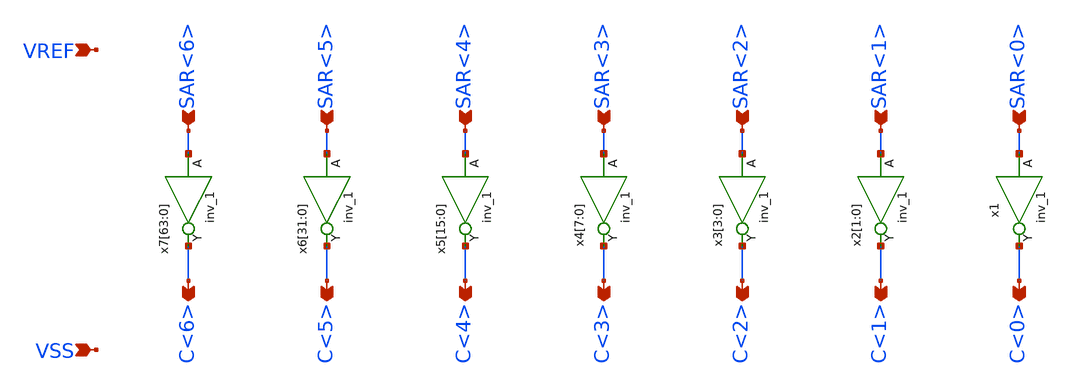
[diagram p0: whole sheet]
** sch_path: module/cdac2/cdac_drv.sch
**.subckt cdac_drv VREF VSS SAR<6> SAR<5> SAR<4> SAR<3> SAR<2> SAR<1> SAR<0> C<6> C<5> C<4> C<3>
*+ C<2> C<1> C<0>
*.ipin VREF
*.ipin VSS
*.ipin SAR<6>
*.ipin SAR<5>
*.ipin SAR<4>
*.ipin SAR<3>
*.ipin SAR<2>
*.ipin SAR<1>
*.ipin SAR<0>
*.opin C<6>
*.opin C<5>
*.opin C<4>
*.opin C<3>
*.opin C<2>
*.opin C<1>
*.opin C<0>
x2[1] SAR<1> VSS VSS VDD VREF C<1> sky130_fd_sc_hd__inv_1
x2[0] SAR<1> VSS VSS VDD VREF C<1> sky130_fd_sc_hd__inv_1
x1 SAR<0> VSS VSS VDD VPWR C<0> sky130_fd_sc_hd__inv_1
x3[3] SAR<2> VSS VSS VDD VREF C<2> sky130_fd_sc_hd__inv_1
x3[2] SAR<2> VSS VSS VDD VREF C<2> sky130_fd_sc_hd__inv_1
x3[1] SAR<2> VSS VSS VDD VREF C<2> sky130_fd_sc_hd__inv_1
x3[0] SAR<2> VSS VSS VDD VREF C<2> sky130_fd_sc_hd__inv_1
x4[7] SAR<3> VSS VSS VDD VREF C<3> sky130_fd_sc_hd__inv_1
x4[6] SAR<3> VSS VSS VDD VREF C<3> sky130_fd_sc_hd__inv_1
x4[5] SAR<3> VSS VSS VDD VREF C<3> sky130_fd_sc_hd__inv_1
x4[4] SAR<3> VSS VSS VDD VREF C<3> sky130_fd_sc_hd__inv_1
x4[3] SAR<3> VSS VSS VDD VREF C<3> sky130_fd_sc_hd__inv_1
x4[2] SAR<3> VSS VSS VDD VREF C<3> sky130_fd_sc_hd__inv_1
x4[1] SAR<3> VSS VSS VDD VREF C<3> sky130_fd_sc_hd__inv_1
x4[0] SAR<3> VSS VSS VDD VREF C<3> sky130_fd_sc_hd__inv_1
x5[15] SAR<4> VSS VSS VDD VREF C<4> sky130_fd_sc_hd__inv_1
x5[14] SAR<4> VSS VSS VDD VREF C<4> sky130_fd_sc_hd__inv_1
x5[13] SAR<4> VSS VSS VDD VREF C<4> sky130_fd_sc_hd__inv_1
x5[12] SAR<4> VSS VSS VDD VREF C<4> sky130_fd_sc_hd__inv_1
x5[11] SAR<4> VSS VSS VDD VREF C<4> sky130_fd_sc_hd__inv_1
x5[10] SAR<4> VSS VSS VDD VREF C<4> sky130_fd_sc_hd__inv_1
x5[9] SAR<4> VSS VSS VDD VREF C<4> sky130_fd_sc_hd__inv_1
x5[8] SAR<4> VSS VSS VDD VREF C<4> sky130_fd_sc_hd__inv_1
x5[7] SAR<4> VSS VSS VDD VREF C<4> sky130_fd_sc_hd__inv_1
x5[6] SAR<4> VSS VSS VDD VREF C<4> sky130_fd_sc_hd__inv_1
x5[5] SAR<4> VSS VSS VDD VREF C<4> sky130_fd_sc_hd__inv_1
x5[4] SAR<4> VSS VSS VDD VREF C<4> sky130_fd_sc_hd__inv_1
x5[3] SAR<4> VSS VSS VDD VREF C<4> sky130_fd_sc_hd__inv_1
x5[2] SAR<4> VSS VSS VDD VREF C<4> sky130_fd_sc_hd__inv_1
x5[1] SAR<4> VSS VSS VDD VREF C<4> sky130_fd_sc_hd__inv_1
x5[0] SAR<4> VSS VSS VDD VREF C<4> sky130_fd_sc_hd__inv_1
x6[31] SAR<5> VSS VSS VDD VREF C<5> sky130_fd_sc_hd__inv_1
x6[30] SAR<5> VSS VSS VDD VREF C<5> sky130_fd_sc_hd__inv_1
x6[29] SAR<5> VSS VSS VDD VREF C<5> sky130_fd_sc_hd__inv_1
x6[28] SAR<5> VSS VSS VDD VREF C<5> sky130_fd_sc_hd__inv_1
x6[27] SAR<5> VSS VSS VDD VREF C<5> sky130_fd_sc_hd__inv_1
x6[26] SAR<5> VSS VSS VDD VREF C<5> sky130_fd_sc_hd__inv_1
x6[25] SAR<5> VSS VSS VDD VREF C<5> sky130_fd_sc_hd__inv_1
x6[24] SAR<5> VSS VSS VDD VREF C<5> sky130_fd_sc_hd__inv_1
x6[23] SAR<5> VSS VSS VDD VREF C<5> sky130_fd_sc_hd__inv_1
x6[22] SAR<5> VSS VSS VDD VREF C<5> sky130_fd_sc_hd__inv_1
x6[21] SAR<5> VSS VSS VDD VREF C<5> sky130_fd_sc_hd__inv_1
x6[20] SAR<5> VSS VSS VDD VREF C<5> sky130_fd_sc_hd__inv_1
x6[19] SAR<5> VSS VSS VDD VREF C<5> sky130_fd_sc_hd__inv_1
x6[18] SAR<5> VSS VSS VDD VREF C<5> sky130_fd_sc_hd__inv_1
x6[17] SAR<5> VSS VSS VDD VREF C<5> sky130_fd_sc_hd__inv_1
x6[16] SAR<5> VSS VSS VDD VREF C<5> sky130_fd_sc_hd__inv_1
x6[15] SAR<5> VSS VSS VDD VREF C<5> sky130_fd_sc_hd__inv_1
x6[14] SAR<5> VSS VSS VDD VREF C<5> sky130_fd_sc_hd__inv_1
x6[13] SAR<5> VSS VSS VDD VREF C<5> sky130_fd_sc_hd__inv_1
x6[12] SAR<5> VSS VSS VDD VREF C<5> sky130_fd_sc_hd__inv_1
x6[11] SAR<5> VSS VSS VDD VREF C<5> sky130_fd_sc_hd__inv_1
x6[10] SAR<5> VSS VSS VDD VREF C<5> sky130_fd_sc_hd__inv_1
x6[9] SAR<5> VSS VSS VDD VREF C<5> sky130_fd_sc_hd__inv_1
x6[8] SAR<5> VSS VSS VDD VREF C<5> sky130_fd_sc_hd__inv_1
x6[7] SAR<5> VSS VSS VDD VREF C<5> sky130_fd_sc_hd__inv_1
x6[6] SAR<5> VSS VSS VDD VREF C<5> sky130_fd_sc_hd__inv_1
x6[5] SAR<5> VSS VSS VDD VREF C<5> sky130_fd_sc_hd__inv_1
x6[4] SAR<5> VSS VSS VDD VREF C<5> sky130_fd_sc_hd__inv_1
x6[3] SAR<5> VSS VSS VDD VREF C<5> sky130_fd_sc_hd__inv_1
x6[2] SAR<5> VSS VSS VDD VREF C<5> sky130_fd_sc_hd__inv_1
x6[1] SAR<5> VSS VSS VDD VREF C<5> sky130_fd_sc_hd__inv_1
x6[0] SAR<5> VSS VSS VDD VREF C<5> sky130_fd_sc_hd__inv_1
x7[63] SAR<6> VSS VSS VDD VREF C<6> sky130_fd_sc_hd__inv_1
x7[62] SAR<6> VSS VSS VDD VREF C<6> sky130_fd_sc_hd__inv_1
x7[61] SAR<6> VSS VSS VDD VREF C<6> sky130_fd_sc_hd__inv_1
x7[60] SAR<6> VSS VSS VDD VREF C<6> sky130_fd_sc_hd__inv_1
x7[59] SAR<6> VSS VSS VDD VREF C<6> sky130_fd_sc_hd__inv_1
x7[58] SAR<6> VSS VSS VDD VREF C<6> sky130_fd_sc_hd__inv_1
x7[57] SAR<6> VSS VSS VDD VREF C<6> sky130_fd_sc_hd__inv_1
x7[56] SAR<6> VSS VSS VDD VREF C<6> sky130_fd_sc_hd__inv_1
x7[55] SAR<6> VSS VSS VDD VREF C<6> sky130_fd_sc_hd__inv_1
x7[54] SAR<6> VSS VSS VDD VREF C<6> sky130_fd_sc_hd__inv_1
x7[53] SAR<6> VSS VSS VDD VREF C<6> sky130_fd_sc_hd__inv_1
x7[52] SAR<6> VSS VSS VDD VREF C<6> sky130_fd_sc_hd__inv_1
x7[51] SAR<6> VSS VSS VDD VREF C<6> sky130_fd_sc_hd__inv_1
x7[50] SAR<6> VSS VSS VDD VREF C<6> sky130_fd_sc_hd__inv_1
x7[49] SAR<6> VSS VSS VDD VREF C<6> sky130_fd_sc_hd__inv_1
x7[48] SAR<6> VSS VSS VDD VREF C<6> sky130_fd_sc_hd__inv_1
x7[47] SAR<6> VSS VSS VDD VREF C<6> sky130_fd_sc_hd__inv_1
x7[46] SAR<6> VSS VSS VDD VREF C<6> sky130_fd_sc_hd__inv_1
x7[45] SAR<6> VSS VSS VDD VREF C<6> sky130_fd_sc_hd__inv_1
x7[44] SAR<6> VSS VSS VDD VREF C<6> sky130_fd_sc_hd__inv_1
x7[43] SAR<6> VSS VSS VDD VREF C<6> sky130_fd_sc_hd__inv_1
x7[42] SAR<6> VSS VSS VDD VREF C<6> sky130_fd_sc_hd__inv_1
x7[41] SAR<6> VSS VSS VDD VREF C<6> sky130_fd_sc_hd__inv_1
x7[40] SAR<6> VSS VSS VDD VREF C<6> sky130_fd_sc_hd__inv_1
x7[39] SAR<6> VSS VSS VDD VREF C<6> sky130_fd_sc_hd__inv_1
x7[38] SAR<6> VSS VSS VDD VREF C<6> sky130_fd_sc_hd__inv_1
x7[37] SAR<6> VSS VSS VDD VREF C<6> sky130_fd_sc_hd__inv_1
x7[36] SAR<6> VSS VSS VDD VREF C<6> sky130_fd_sc_hd__inv_1
x7[35] SAR<6> VSS VSS VDD VREF C<6> sky130_fd_sc_hd__inv_1
x7[34] SAR<6> VSS VSS VDD VREF C<6> sky130_fd_sc_hd__inv_1
x7[33] SAR<6> VSS VSS VDD VREF C<6> sky130_fd_sc_hd__inv_1
x7[32] SAR<6> VSS VSS VDD VREF C<6> sky130_fd_sc_hd__inv_1
x7[31] SAR<6> VSS VSS VDD VREF C<6> sky130_fd_sc_hd__inv_1
x7[30] SAR<6> VSS VSS VDD VREF C<6> sky130_fd_sc_hd__inv_1
x7[29] SAR<6> VSS VSS VDD VREF C<6> sky130_fd_sc_hd__inv_1
x7[28] SAR<6> VSS VSS VDD VREF C<6> sky130_fd_sc_hd__inv_1
x7[27] SAR<6> VSS VSS VDD VREF C<6> sky130_fd_sc_hd__inv_1
x7[26] SAR<6> VSS VSS VDD VREF C<6> sky130_fd_sc_hd__inv_1
x7[25] SAR<6> VSS VSS VDD VREF C<6> sky130_fd_sc_hd__inv_1
x7[24] SAR<6> VSS VSS VDD VREF C<6> sky130_fd_sc_hd__inv_1
x7[23] SAR<6> VSS VSS VDD VREF C<6> sky130_fd_sc_hd__inv_1
x7[22] SAR<6> VSS VSS VDD VREF C<6> sky130_fd_sc_hd__inv_1
x7[21] SAR<6> VSS VSS VDD VREF C<6> sky130_fd_sc_hd__inv_1
x7[20] SAR<6> VSS VSS VDD VREF C<6> sky130_fd_sc_hd__inv_1
x7[19] SAR<6> VSS VSS VDD VREF C<6> sky130_fd_sc_hd__inv_1
x7[18] SAR<6> VSS VSS VDD VREF C<6> sky130_fd_sc_hd__inv_1
x7[17] SAR<6> VSS VSS VDD VREF C<6> sky130_fd_sc_hd__inv_1
x7[16] SAR<6> VSS VSS VDD VREF C<6> sky130_fd_sc_hd__inv_1
x7[15] SAR<6> VSS VSS VDD VREF C<6> sky130_fd_sc_hd__inv_1
x7[14] SAR<6> VSS VSS VDD VREF C<6> sky130_fd_sc_hd__inv_1
x7[13] SAR<6> VSS VSS VDD VREF C<6> sky130_fd_sc_hd__inv_1
x7[12] SAR<6> VSS VSS VDD VREF C<6> sky130_fd_sc_hd__inv_1
x7[11] SAR<6> VSS VSS VDD VREF C<6> sky130_fd_sc_hd__inv_1
x7[10] SAR<6> VSS VSS VDD VREF C<6> sky130_fd_sc_hd__inv_1
x7[9] SAR<6> VSS VSS VDD VREF C<6> sky130_fd_sc_hd__inv_1
x7[8] SAR<6> VSS VSS VDD VREF C<6> sky130_fd_sc_hd__inv_1
x7[7] SAR<6> VSS VSS VDD VREF C<6> sky130_fd_sc_hd__inv_1
x7[6] SAR<6> VSS VSS VDD VREF C<6> sky130_fd_sc_hd__inv_1
x7[5] SAR<6> VSS VSS VDD VREF C<6> sky130_fd_sc_hd__inv_1
x7[4] SAR<6> VSS VSS VDD VREF C<6> sky130_fd_sc_hd__inv_1
x7[3] SAR<6> VSS VSS VDD VREF C<6> sky130_fd_sc_hd__inv_1
x7[2] SAR<6> VSS VSS VDD VREF C<6> sky130_fd_sc_hd__inv_1
x7[1] SAR<6> VSS VSS VDD VREF C<6> sky130_fd_sc_hd__inv_1
x7[0] SAR<6> VSS VSS VDD VREF C<6> sky130_fd_sc_hd__inv_1
**.ends
.end
